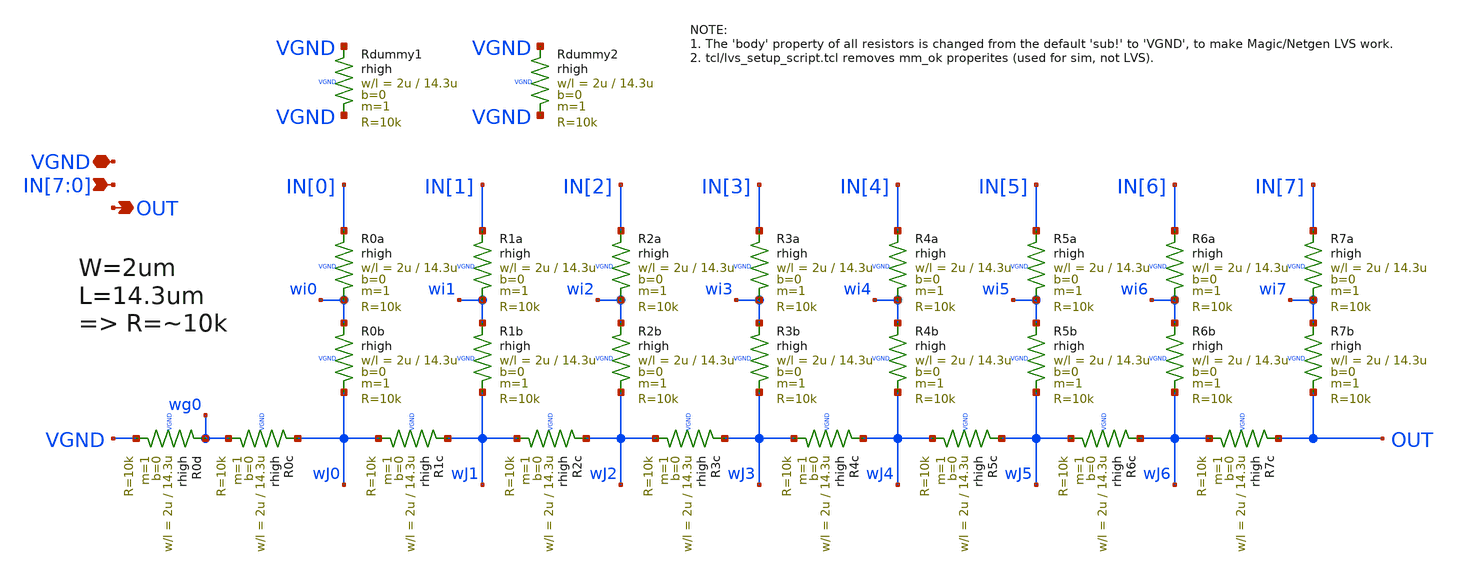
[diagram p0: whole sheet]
** sch_path: xschem/r2r_dac.sch
**.subckt r2r_dac IN[7],IN[6],IN[5],IN[4],IN[3],IN[2],IN[1],IN[0] VGND OUT
*.ipin IN[7],IN[6],IN[5],IN[4],IN[3],IN[2],IN[1],IN[0]
*.iopin VGND
*.opin OUT
XR0a IN[0] wi0 VGND rhigh w=2u l=14.3u m=1 b=0 mm_ok=1
XR0b wi0 wJ0 VGND rhigh w=2u l=14.3u m=1 b=0 mm_ok=1
XR1c wJ1 wJ0 VGND rhigh w=2u l=14.3u m=1 b=0 mm_ok=1
XR0c wJ0 wg0 VGND rhigh w=2u l=14.3u m=1 b=0 mm_ok=1
XR0d wg0 VGND VGND rhigh w=2u l=14.3u m=1 b=0 mm_ok=1
XR1a IN[1] wi1 VGND rhigh w=2u l=14.3u m=1 b=0 mm_ok=1
XR1b wi1 wJ1 VGND rhigh w=2u l=14.3u m=1 b=0 mm_ok=1
XR2c wJ2 wJ1 VGND rhigh w=2u l=14.3u m=1 b=0 mm_ok=1
XR2a IN[2] wi2 VGND rhigh w=2u l=14.3u m=1 b=0 mm_ok=1
XR2b wi2 wJ2 VGND rhigh w=2u l=14.3u m=1 b=0 mm_ok=1
XR3c wJ3 wJ2 VGND rhigh w=2u l=14.3u m=1 b=0 mm_ok=1
XR3a IN[3] wi3 VGND rhigh w=2u l=14.3u m=1 b=0 mm_ok=1
XR3b wi3 wJ3 VGND rhigh w=2u l=14.3u m=1 b=0 mm_ok=1
XR4c wJ4 wJ3 VGND rhigh w=2u l=14.3u m=1 b=0 mm_ok=1
XR4a IN[4] wi4 VGND rhigh w=2u l=14.3u m=1 b=0 mm_ok=1
XR4b wi4 wJ4 VGND rhigh w=2u l=14.3u m=1 b=0 mm_ok=1
XR5c wJ5 wJ4 VGND rhigh w=2u l=14.3u m=1 b=0 mm_ok=1
XR5a IN[5] wi5 VGND rhigh w=2u l=14.3u m=1 b=0 mm_ok=1
XR5b wi5 wJ5 VGND rhigh w=2u l=14.3u m=1 b=0 mm_ok=1
XR6c wJ6 wJ5 VGND rhigh w=2u l=14.3u m=1 b=0 mm_ok=1
XR6a IN[6] wi6 VGND rhigh w=2u l=14.3u m=1 b=0 mm_ok=1
XR6b wi6 wJ6 VGND rhigh w=2u l=14.3u m=1 b=0 mm_ok=1
XR7c OUT wJ6 VGND rhigh w=2u l=14.3u m=1 b=0 mm_ok=1
XR7a IN[7] wi7 VGND rhigh w=2u l=14.3u m=1 b=0 mm_ok=1
XR7b wi7 OUT VGND rhigh w=2u l=14.3u m=1 b=0 mm_ok=1
XRdummy1 VGND VGND VGND rhigh w=2u l=14.3u m=1 b=0 mm_ok=1
XRdummy2 VGND VGND VGND rhigh w=2u l=14.3u m=1 b=0 mm_ok=1
**.ends
.end
